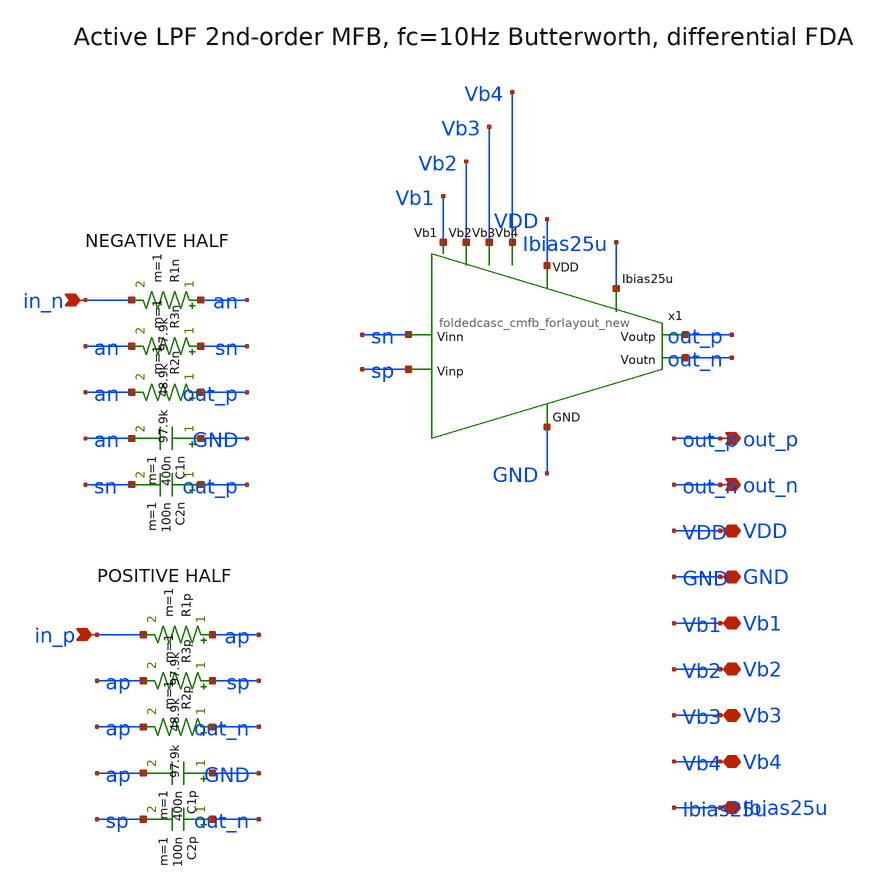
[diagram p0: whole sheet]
** sch_path: ps-filters/lpf.sch
**.subckt lpf in_p in_n out_p out_n VDD GND Vb1 Vb2 Vb3 Vb4 Ibias25u
*.ipin in_p
*.ipin in_n
*.opin out_p
*.opin out_n
*.iopin VDD
*.iopin GND
*.iopin Vb1
*.iopin Vb2
*.iopin Vb3
*.iopin Vb4
*.iopin Ibias25u
R1p ap in_p 97.9k m=1
R3p sp ap 48.9k m=1
R2p out_n ap 97.9k m=1
C1p GND ap 400n m=1
C2p out_n sp 100n m=1
R1n an in_n 97.9k m=1
R3n sn an 48.9k m=1
R2n out_p an 97.9k m=1
C1n GND an 400n m=1
C2n out_p sn 100n m=1
x1 VDD Vb2 out_p out_n Vb1 Ibias25u sn GND sp Vb3 Vb4 foldedcasc_cmfb_forlayout_new
**.ends

* expanding   symbol:  chipathon-2026-ppg/jz_fda2/xschem/foldedcasc_cmfb_forlayout_new.sym # of
*+ pins=11
** sym_path: jz_fda2/xschem/foldedcasc_cmfb_forlayout_new.sym
** sch_path: jz_fda2/xschem/foldedcasc_cmfb_forlayout_new.sch
.subckt foldedcasc_cmfb_forlayout_new VDD Vb2 Voutp Voutn Vb1 Ibias25u Vinn GND Vinp Vb3 Vb4
*.ipin VDD
*.opin Voutp
*.ipin Vinn
*.ipin Ibias25u
*.ipin GND
*.ipin Vinp
*.opin Voutn
*.ipin Vb4
*.ipin Vb1
*.ipin Vb2
*.ipin Vb3
XM5 net1 Vb3 GND GND nfet_03v3 L=0.56u W=26u nf=4 ad='int((nf+1)/2) * W/nf * 0.18u' as='int((nf+2)/2) * W/nf * 0.18u'
+ pd='2*int((nf+1)/2) * (W/nf + 0.18u)' ps='2*int((nf+2)/2) * (W/nf + 0.18u)' nrd='0.18u / W' nrs='0.18u / W'
+ sa=0 sb=0 sd=0 m=1
XM6 Voutn Vb2 net2 GND nfet_03v3 L=0.56u W=35u nf=2 ad='int((nf+1)/2) * W/nf * 0.18u' as='int((nf+2)/2) * W/nf * 0.18u'
+ pd='2*int((nf+1)/2) * (W/nf + 0.18u)' ps='2*int((nf+2)/2) * (W/nf + 0.18u)' nrd='0.18u / W' nrs='0.18u / W'
+ sa=0 sb=0 sd=0 m=1
XM7 Voutp Vb2 net1 GND nfet_03v3 L=0.56u W=35u nf=2 ad='int((nf+1)/2) * W/nf * 0.18u' as='int((nf+2)/2) * W/nf * 0.18u'
+ pd='2*int((nf+1)/2) * (W/nf + 0.18u)' ps='2*int((nf+2)/2) * (W/nf + 0.18u)' nrd='0.18u / W' nrs='0.18u / W'
+ sa=0 sb=0 sd=0 m=1
XM8 Voutn Vb1 net3 VDD pfet_03v3 L=0.56u W=24u nf=5 ad='int((nf+1)/2) * W/nf * 0.18u' as='int((nf+2)/2) * W/nf * 0.18u'
+ pd='2*int((nf+1)/2) * (W/nf + 0.18u)' ps='2*int((nf+2)/2) * (W/nf + 0.18u)' nrd='0.18u / W' nrs='0.18u / W'
+ sa=0 sb=0 sd=0 m=1
XM9 Voutp Vb1 net4 VDD pfet_03v3 L=0.56u W=24u nf=5 ad='int((nf+1)/2) * W/nf * 0.18u' as='int((nf+2)/2) * W/nf * 0.18u'
+ pd='2*int((nf+1)/2) * (W/nf + 0.18u)' ps='2*int((nf+2)/2) * (W/nf + 0.18u)' nrd='0.18u / W' nrs='0.18u / W'
+ sa=0 sb=0 sd=0 m=1
XM10 net3 Vb4 VDD VDD pfet_03v3 L=0.56u W=23u nf=4 ad='int((nf+1)/2) * W/nf * 0.18u' as='int((nf+2)/2) * W/nf * 0.18u'
+ pd='2*int((nf+1)/2) * (W/nf + 0.18u)' ps='2*int((nf+2)/2) * (W/nf + 0.18u)' nrd='0.18u / W' nrs='0.18u / W'
+ sa=0 sb=0 sd=0 m=1
XM11 net4 Vb4 VDD VDD pfet_03v3 L=0.56u W=23u nf=4 ad='int((nf+1)/2) * W/nf * 0.18u' as='int((nf+2)/2) * W/nf * 0.18u'
+ pd='2*int((nf+1)/2) * (W/nf + 0.18u)' ps='2*int((nf+2)/2) * (W/nf + 0.18u)' nrd='0.18u / W' nrs='0.18u / W'
+ sa=0 sb=0 sd=0 m=1
XM1 net1 Vinn net5 VDD pfet_03v3 L=0.28u W=3.45u nf=1 ad='int((nf+1)/2) * W/nf * 0.18u' as='int((nf+2)/2) * W/nf * 0.18u'
+ pd='2*int((nf+1)/2) * (W/nf + 0.18u)' ps='2*int((nf+2)/2) * (W/nf + 0.18u)' nrd='0.18u / W' nrs='0.18u / W'
+ sa=0 sb=0 sd=0 m=1
XM2 net2 Vinp net5 VDD pfet_03v3 L=0.28u W=3.45u nf=1 ad='int((nf+1)/2) * W/nf * 0.18u' as='int((nf+2)/2) * W/nf * 0.18u'
+ pd='2*int((nf+1)/2) * (W/nf + 0.18u)' ps='2*int((nf+2)/2) * (W/nf + 0.18u)' nrd='0.18u / W' nrs='0.18u / W'
+ sa=0 sb=0 sd=0 m=1
XM3 net5 Ibias25u net6 VDD pfet_03v3 L=0.28u W=4.9u nf=2 ad='int((nf+1)/2) * W/nf * 0.18u' as='int((nf+2)/2) * W/nf * 0.18u'
+ pd='2*int((nf+1)/2) * (W/nf + 0.18u)' ps='2*int((nf+2)/2) * (W/nf + 0.18u)' nrd='0.18u / W' nrs='0.18u / W'
+ sa=0 sb=0 sd=0 m=1
XM12 Ibias25u Ibias25u VDD VDD pfet_03v3 L=0.28u W=2.27u nf=1 ad='int((nf+1)/2) * W/nf * 0.18u' as='int((nf+2)/2) * W/nf * 0.18u'
+ pd='2*int((nf+1)/2) * (W/nf + 0.18u)' ps='2*int((nf+2)/2) * (W/nf + 0.18u)' nrd='0.18u / W' nrs='0.18u / W'
+ sa=0 sb=0 sd=0 m=1
XM13 net6 Voutp VDD VDD pfet_03v3 L=0.28u W=30u nf=3 ad='int((nf+1)/2) * W/nf * 0.18u' as='int((nf+2)/2) * W/nf * 0.18u'
+ pd='2*int((nf+1)/2) * (W/nf + 0.18u)' ps='2*int((nf+2)/2) * (W/nf + 0.18u)' nrd='0.18u / W' nrs='0.18u / W'
+ sa=0 sb=0 sd=0 m=1
XM14 net6 Voutn VDD VDD pfet_03v3 L=0.28u W=30u nf=3 ad='int((nf+1)/2) * W/nf * 0.18u' as='int((nf+2)/2) * W/nf * 0.18u'
+ pd='2*int((nf+1)/2) * (W/nf + 0.18u)' ps='2*int((nf+2)/2) * (W/nf + 0.18u)' nrd='0.18u / W' nrs='0.18u / W'
+ sa=0 sb=0 sd=0 m=1
XM4 net2 Vb3 GND GND nfet_03v3 L=0.56u W=26u nf=4 ad='int((nf+1)/2) * W/nf * 0.18u' as='int((nf+2)/2) * W/nf * 0.18u'
+ pd='2*int((nf+1)/2) * (W/nf + 0.18u)' ps='2*int((nf+2)/2) * (W/nf + 0.18u)' nrd='0.18u / W' nrs='0.18u / W'
+ sa=0 sb=0 sd=0 m=1
XM15 VDD VDD VDD VDD pfet_03v3 L=0.28u W=2.27u nf=1 ad='int((nf+1)/2) * W/nf * 0.18u' as='int((nf+2)/2) * W/nf * 0.18u'
+ pd='2*int((nf+1)/2) * (W/nf + 0.18u)' ps='2*int((nf+2)/2) * (W/nf + 0.18u)' nrd='0.18u / W' nrs='0.18u / W'
+ sa=0 sb=0 sd=0 m=1
.ends

.end
